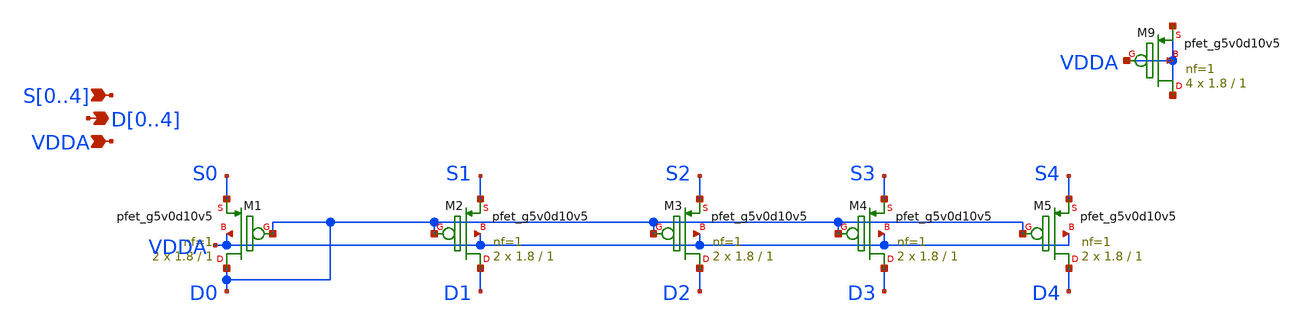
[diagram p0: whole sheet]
** sch_path: xschem/cm2_pcell2.sch
**.subckt cm2_pcell2 D0,D1,D2,D3,D4 VDDA S0,S1,S2,S3,S4
*.opin D0,D1,D2,D3,D4
*.ipin VDDA
*.ipin S0,S1,S2,S3,S4
XM1 D0 D0 S0 VDDA sky130_fd_pr__pfet_g5v0d10v5 L=1 W=1.8 nf=1 ad='int((nf+1)/2) * W/nf * 0.29' as='int((nf+2)/2) * W/nf * 0.29'
+ pd='2*int((nf+1)/2) * (W/nf + 0.29)' ps='2*int((nf+2)/2) * (W/nf + 0.29)' nrd='0.29 / W' nrs='0.29 / W'
+ sa=0 sb=0 sd=0 mult=2 m=2
XM9 VDDA VDDA VDDA VDDA sky130_fd_pr__pfet_g5v0d10v5 L=1 W=1.8 nf=1 ad='int((nf+1)/2) * W/nf * 0.29'
+ as='int((nf+2)/2) * W/nf * 0.29' pd='2*int((nf+1)/2) * (W/nf + 0.29)' ps='2*int((nf+2)/2) * (W/nf + 0.29)'
+ nrd='0.29 / W' nrs='0.29 / W' sa=0 sb=0 sd=0 mult=4 m=4
XM2 D1 D0 S1 VDDA sky130_fd_pr__pfet_g5v0d10v5 L=1 W=1.8 nf=1 ad='int((nf+1)/2) * W/nf * 0.29' as='int((nf+2)/2) * W/nf * 0.29'
+ pd='2*int((nf+1)/2) * (W/nf + 0.29)' ps='2*int((nf+2)/2) * (W/nf + 0.29)' nrd='0.29 / W' nrs='0.29 / W'
+ sa=0 sb=0 sd=0 mult=2 m=2
XM3 D2 D0 S2 VDDA sky130_fd_pr__pfet_g5v0d10v5 L=1 W=1.8 nf=1 ad='int((nf+1)/2) * W/nf * 0.29' as='int((nf+2)/2) * W/nf * 0.29'
+ pd='2*int((nf+1)/2) * (W/nf + 0.29)' ps='2*int((nf+2)/2) * (W/nf + 0.29)' nrd='0.29 / W' nrs='0.29 / W'
+ sa=0 sb=0 sd=0 mult=2 m=2
XM4 D3 D0 S3 VDDA sky130_fd_pr__pfet_g5v0d10v5 L=1 W=1.8 nf=1 ad='int((nf+1)/2) * W/nf * 0.29' as='int((nf+2)/2) * W/nf * 0.29'
+ pd='2*int((nf+1)/2) * (W/nf + 0.29)' ps='2*int((nf+2)/2) * (W/nf + 0.29)' nrd='0.29 / W' nrs='0.29 / W'
+ sa=0 sb=0 sd=0 mult=2 m=2
XM5 D4 D0 S4 VDDA sky130_fd_pr__pfet_g5v0d10v5 L=1 W=1.8 nf=1 ad='int((nf+1)/2) * W/nf * 0.29' as='int((nf+2)/2) * W/nf * 0.29'
+ pd='2*int((nf+1)/2) * (W/nf + 0.29)' ps='2*int((nf+2)/2) * (W/nf + 0.29)' nrd='0.29 / W' nrs='0.29 / W'
+ sa=0 sb=0 sd=0 mult=2 m=2
**.ends
.end
